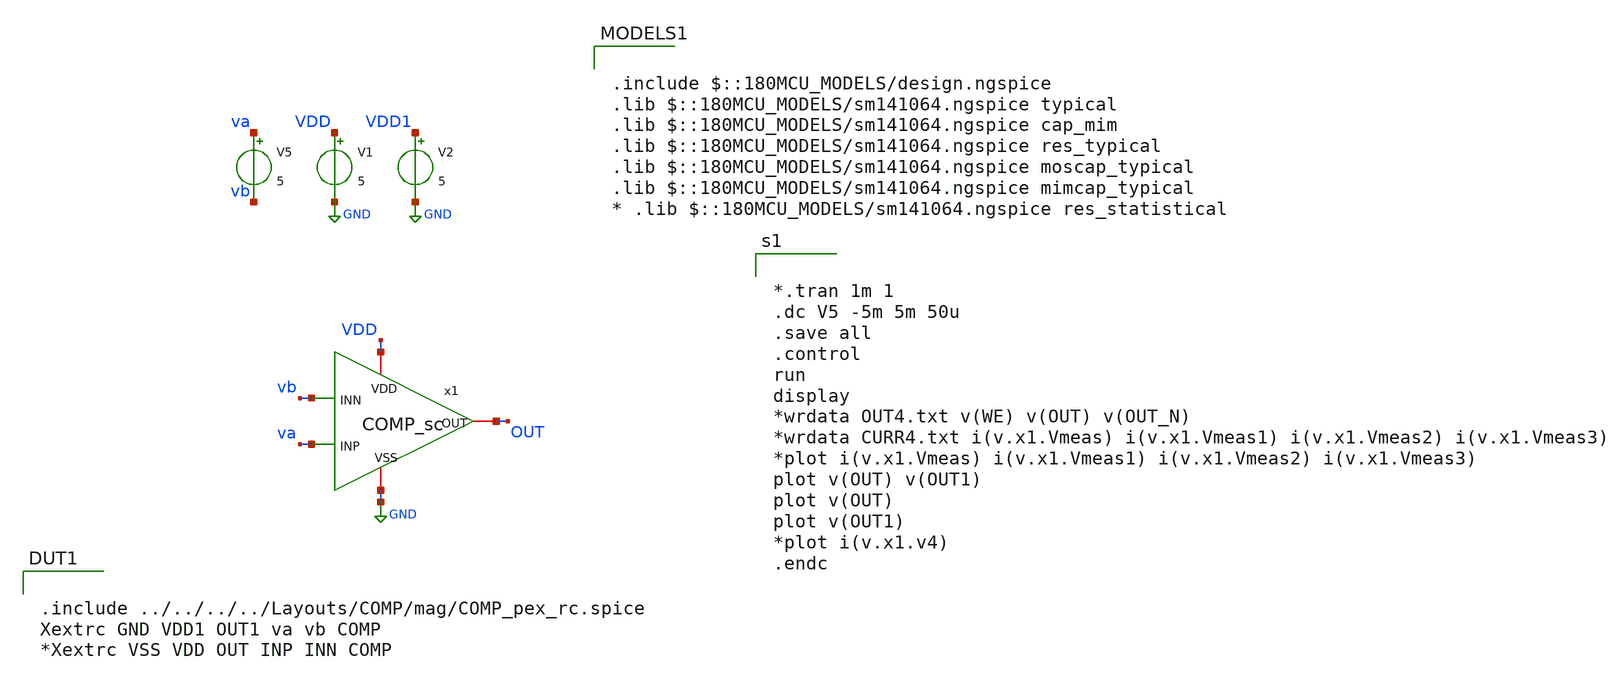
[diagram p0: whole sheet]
** sch_path: FINAL/XSCHEM/TEST/test_comp_ac.sch
**.subckt test_comp_ac
V1 VDD GND 5
V5 va vb 5
x1 VDD vb OUT va GND COMP_sc
V2 VDD1 GND 5
**** begin user architecture code


*.tran 1m 1
.dc V5 -5m 5m 50u
.save all
.control
run
display
*wrdata OUT4.txt v(WE) v(OUT) v(OUT_N)
*wrdata CURR4.txt i(v.x1.Vmeas) i(v.x1.Vmeas1) i(v.x1.Vmeas2) i(v.x1.Vmeas3)
*plot i(v.x1.Vmeas) i(v.x1.Vmeas1) i(v.x1.Vmeas2) i(v.x1.Vmeas3)
plot v(OUT) v(OUT1)
plot v(OUT)
plot v(OUT1)
*plot i(v.x1.v4)
.endc



.include $::180MCU_MODELS/design.ngspice
.lib $::180MCU_MODELS/sm141064.ngspice typical
.lib $::180MCU_MODELS/sm141064.ngspice cap_mim
.lib $::180MCU_MODELS/sm141064.ngspice res_typical
.lib $::180MCU_MODELS/sm141064.ngspice moscap_typical
.lib $::180MCU_MODELS/sm141064.ngspice mimcap_typical
* .lib $::180MCU_MODELS/sm141064.ngspice res_statistical


.include ../../../../Layouts/COMP/mag/COMP_pex_rc.spice
Xextrc GND VDD1 OUT1 va vb COMP
*Xextrc VSS VDD OUT INP INN COMP


**** end user architecture code
**.ends
.GLOBAL GND
.end
